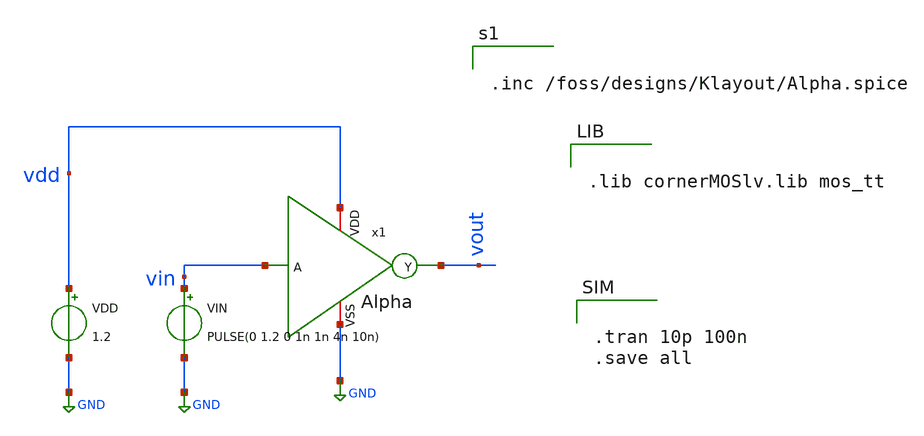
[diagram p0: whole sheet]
** sch_path: BTDay2-Ex/Test_alpha.sch
**.subckt Test_alpha
VIN vin GND PULSE(0 1.2 0 1n 1n 4n 10n)
VDD vdd GND 1.2
x1 vdd vin vout GND Alpha
**** begin user architecture code


.lib cornerMOSlv.lib mos_tt




.tran 10p 100n
.save all




.inc /foss/designs/Klayout/Alpha.spice


**** end user architecture code
**.ends
.GLOBAL GND
.end
